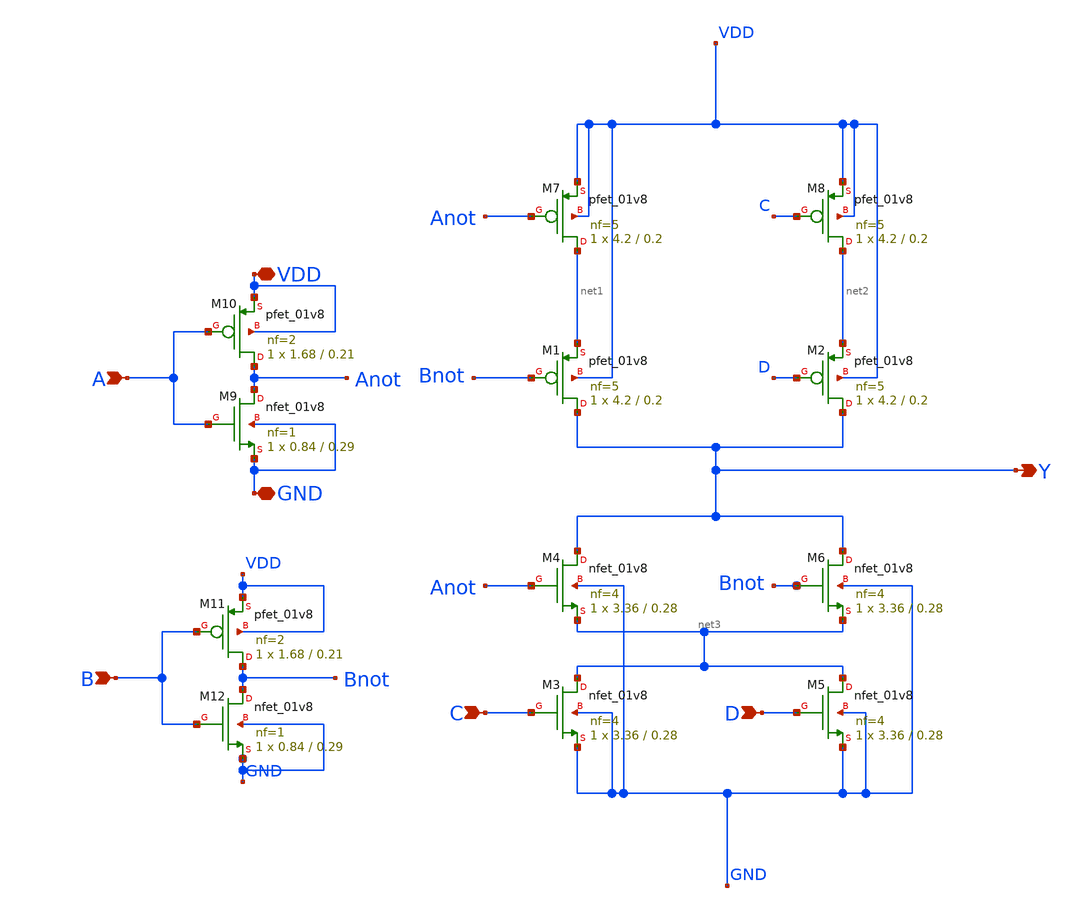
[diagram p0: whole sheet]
** sch_path: cells/MOAI4X4/schematic/moai4x4.sch
**.subckt moai4x4 A VDD GND B D C Y
*.ipin A
*.iopin VDD
*.iopin GND
*.ipin B
*.ipin D
*.ipin C
*.opin Y
XM9 Anot A GND GND sky130_fd_pr__nfet_01v8 L=0.29 W=0.84 nf=1 ad='int((1 + 1)/2) * 0.84 / 1 * 0.29' as='int((1 + 2)/2) * 0.84 / 1 * 0.29'
+ pd='2*int((1 + 1)/2) * (0.84 / 1 + 0.29)' ps='2*int((1 + 2)/2) * (0.84 / 1 + 0.29)' nrd='0.29 / 0.84 '
+ nrs='0.29 / 0.84 ' sa=0 sb=0 sd=0 mult=1 m=1
XM10 Anot A VDD VDD sky130_fd_pr__pfet_01v8 L=0.21 W=1.68 nf=2 ad='int((2 + 1)/2) * 1.68 / 2 * 0.29'
+ as='int((2 + 2)/2) * 1.68 / 2 * 0.29' pd='2*int((2 + 1)/2) * (1.68 / 2 + 0.29)' ps='2*int((2 + 2)/2) * (1.68 / 2 + 0.29)'
+ nrd='0.29 / 1.68 ' nrs='0.29 / 1.68 ' sa=0 sb=0 sd=0 mult=1 m=1
XM4 Y Anot net3 GND sky130_fd_pr__nfet_01v8 L=0.28 W=3.36 nf=4 ad='int((4 + 1)/2) * 3.36 / 4 * 0.29'
+ as='int((4 + 2)/2) * 3.36 / 4 * 0.29' pd='2*int((4 + 1)/2) * (3.36 / 4 + 0.29)' ps='2*int((4 + 2)/2) * (3.36 / 4 + 0.29)'
+ nrd='0.29 / 3.36 ' nrs='0.29 / 3.36 ' sa=0 sb=0 sd=0 mult=1 m=1
XM7 net1 Anot VDD VDD sky130_fd_pr__pfet_01v8 L=0.2 W=4.2 nf=5 ad='int((5 + 1)/2) * 4.2 / 5 * 0.29' as='int((5 + 2)/2) * 4.2 / 5 * 0.29'
+ pd='2*int((5 + 1)/2) * (4.2 / 5 + 0.29)' ps='2*int((5 + 2)/2) * (4.2 / 5 + 0.29)' nrd='0.29 / 4.2 ' nrs='0.29 / 4.2 '
+ sa=0 sb=0 sd=0 mult=1 m=1
XM1 Y Bnot net1 VDD sky130_fd_pr__pfet_01v8 L=0.2 W=4.2 nf=5 ad='int((5 + 1)/2) * 4.2 / 5 * 0.29' as='int((5 + 2)/2) * 4.2 / 5 * 0.29'
+ pd='2*int((5 + 1)/2) * (4.2 / 5 + 0.29)' ps='2*int((5 + 2)/2) * (4.2 / 5 + 0.29)' nrd='0.29 / 4.2 ' nrs='0.29 / 4.2 '
+ sa=0 sb=0 sd=0 mult=1 m=1
XM2 Y D net2 VDD sky130_fd_pr__pfet_01v8 L=0.2 W=4.2 nf=5 ad='int((5 + 1)/2) * 4.2 / 5 * 0.29' as='int((5 + 2)/2) * 4.2 / 5 * 0.29'
+ pd='2*int((5 + 1)/2) * (4.2 / 5 + 0.29)' ps='2*int((5 + 2)/2) * (4.2 / 5 + 0.29)' nrd='0.29 / 4.2 ' nrs='0.29 / 4.2 '
+ sa=0 sb=0 sd=0 mult=1 m=1
XM8 net2 C VDD VDD sky130_fd_pr__pfet_01v8 L=0.2 W=4.2 nf=5 ad='int((5 + 1)/2) * 4.2 / 5 * 0.29' as='int((5 + 2)/2) * 4.2 / 5 * 0.29'
+ pd='2*int((5 + 1)/2) * (4.2 / 5 + 0.29)' ps='2*int((5 + 2)/2) * (4.2 / 5 + 0.29)' nrd='0.29 / 4.2 ' nrs='0.29 / 4.2 '
+ sa=0 sb=0 sd=0 mult=1 m=1
XM11 Bnot B VDD VDD sky130_fd_pr__pfet_01v8 L=0.21 W=1.68 nf=2 ad='int((2 + 1)/2) * 1.68 / 2 * 0.29'
+ as='int((2 + 2)/2) * 1.68 / 2 * 0.29' pd='2*int((2 + 1)/2) * (1.68 / 2 + 0.29)' ps='2*int((2 + 2)/2) * (1.68 / 2 + 0.29)'
+ nrd='0.29 / 1.68 ' nrs='0.29 / 1.68 ' sa=0 sb=0 sd=0 mult=1 m=1
XM12 Bnot B GND GND sky130_fd_pr__nfet_01v8 L=0.29 W=0.84 nf=1 ad='int((1 + 1)/2) * 0.84 / 1 * 0.29'
+ as='int((1 + 2)/2) * 0.84 / 1 * 0.29' pd='2*int((1 + 1)/2) * (0.84 / 1 + 0.29)' ps='2*int((1 + 2)/2) * (0.84 / 1 + 0.29)'
+ nrd='0.29 / 0.84 ' nrs='0.29 / 0.84 ' sa=0 sb=0 sd=0 mult=1 m=1
XM3 net3 C GND GND sky130_fd_pr__nfet_01v8 L=0.28 W=3.36 nf=4 ad='int((4 + 1)/2) * 3.36 / 4 * 0.29' as='int((4 + 2)/2) * 3.36 / 4 * 0.29'
+ pd='2*int((4 + 1)/2) * (3.36 / 4 + 0.29)' ps='2*int((4 + 2)/2) * (3.36 / 4 + 0.29)' nrd='0.29 / 3.36 '
+ nrs='0.29 / 3.36 ' sa=0 sb=0 sd=0 mult=1 m=1
XM5 net3 D GND GND sky130_fd_pr__nfet_01v8 L=0.28 W=3.36 nf=4 ad='int((4 + 1)/2) * 3.36 / 4 * 0.29' as='int((4 + 2)/2) * 3.36 / 4 * 0.29'
+ pd='2*int((4 + 1)/2) * (3.36 / 4 + 0.29)' ps='2*int((4 + 2)/2) * (3.36 / 4 + 0.29)' nrd='0.29 / 3.36 '
+ nrs='0.29 / 3.36 ' sa=0 sb=0 sd=0 mult=1 m=1
XM6 Y Bnot net3 GND sky130_fd_pr__nfet_01v8 L=0.28 W=3.36 nf=4 ad='int((4 + 1)/2) * 3.36 / 4 * 0.29'
+ as='int((4 + 2)/2) * 3.36 / 4 * 0.29' pd='2*int((4 + 1)/2) * (3.36 / 4 + 0.29)' ps='2*int((4 + 2)/2) * (3.36 / 4 + 0.29)'
+ nrd='0.29 / 3.36 ' nrs='0.29 / 3.36 ' sa=0 sb=0 sd=0 mult=1 m=1
**.ends
.end
